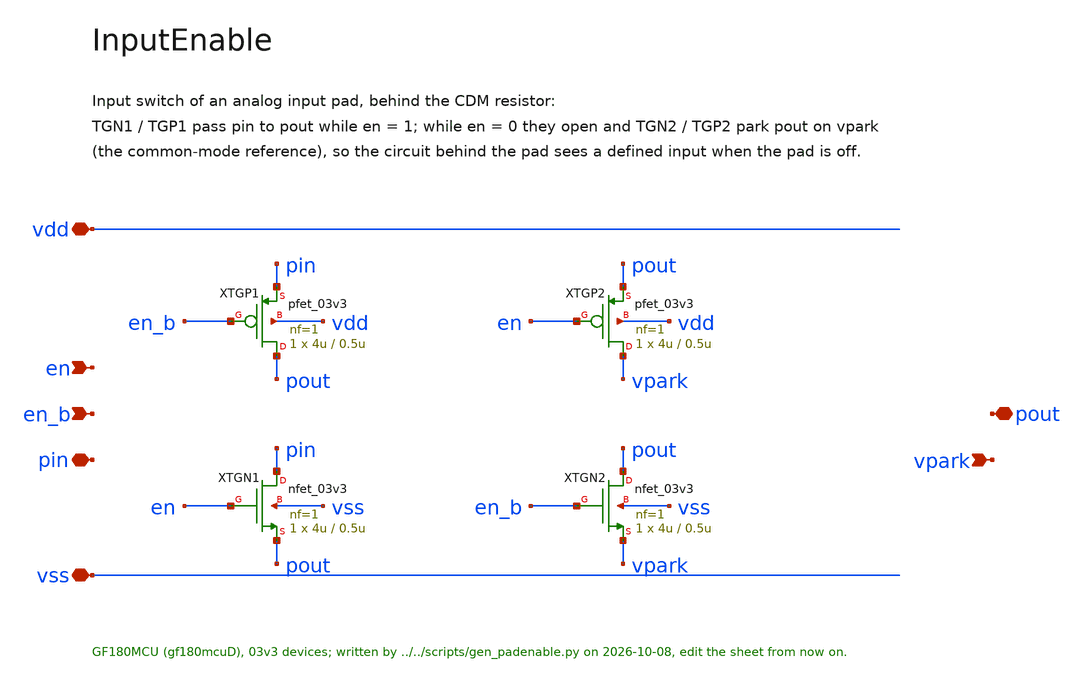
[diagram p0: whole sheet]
** sch_path: macros/PadEnable/schematic/xschem/InputEnable.sch
**.subckt InputEnable vdd vss en en_b pin pout vpark
*.iopin vdd
*.iopin vss
*.ipin en
*.ipin en_b
*.iopin pin
*.iopin pout
*.ipin vpark
XTGP1 pout en_b pin vdd pfet_03v3 L=0.5u W=4u nf=1 ad='int((nf+1)/2) * W/nf * 0.18u' as='int((nf+2)/2) * W/nf * 0.18u'
+ pd='2*int((nf+1)/2) * (W/nf + 0.18u)' ps='2*int((nf+2)/2) * (W/nf + 0.18u)' nrd='0.18u / W' nrs='0.18u / W'
+ sa=0 sb=0 sd=0 m=1
XTGN1 pin en pout vss nfet_03v3 L=0.5u W=4u nf=1 ad='int((nf+1)/2) * W/nf * 0.18u' as='int((nf+2)/2) * W/nf * 0.18u'
+ pd='2*int((nf+1)/2) * (W/nf + 0.18u)' ps='2*int((nf+2)/2) * (W/nf + 0.18u)' nrd='0.18u / W' nrs='0.18u / W'
+ sa=0 sb=0 sd=0 m=1
XTGP2 vpark en pout vdd pfet_03v3 L=0.5u W=4u nf=1 ad='int((nf+1)/2) * W/nf * 0.18u' as='int((nf+2)/2) * W/nf * 0.18u'
+ pd='2*int((nf+1)/2) * (W/nf + 0.18u)' ps='2*int((nf+2)/2) * (W/nf + 0.18u)' nrd='0.18u / W' nrs='0.18u / W'
+ sa=0 sb=0 sd=0 m=1
XTGN2 pout en_b vpark vss nfet_03v3 L=0.5u W=4u nf=1 ad='int((nf+1)/2) * W/nf * 0.18u' as='int((nf+2)/2) * W/nf * 0.18u'
+ pd='2*int((nf+1)/2) * (W/nf + 0.18u)' ps='2*int((nf+2)/2) * (W/nf + 0.18u)' nrd='0.18u / W' nrs='0.18u / W'
+ sa=0 sb=0 sd=0 m=1
**.ends
.end
